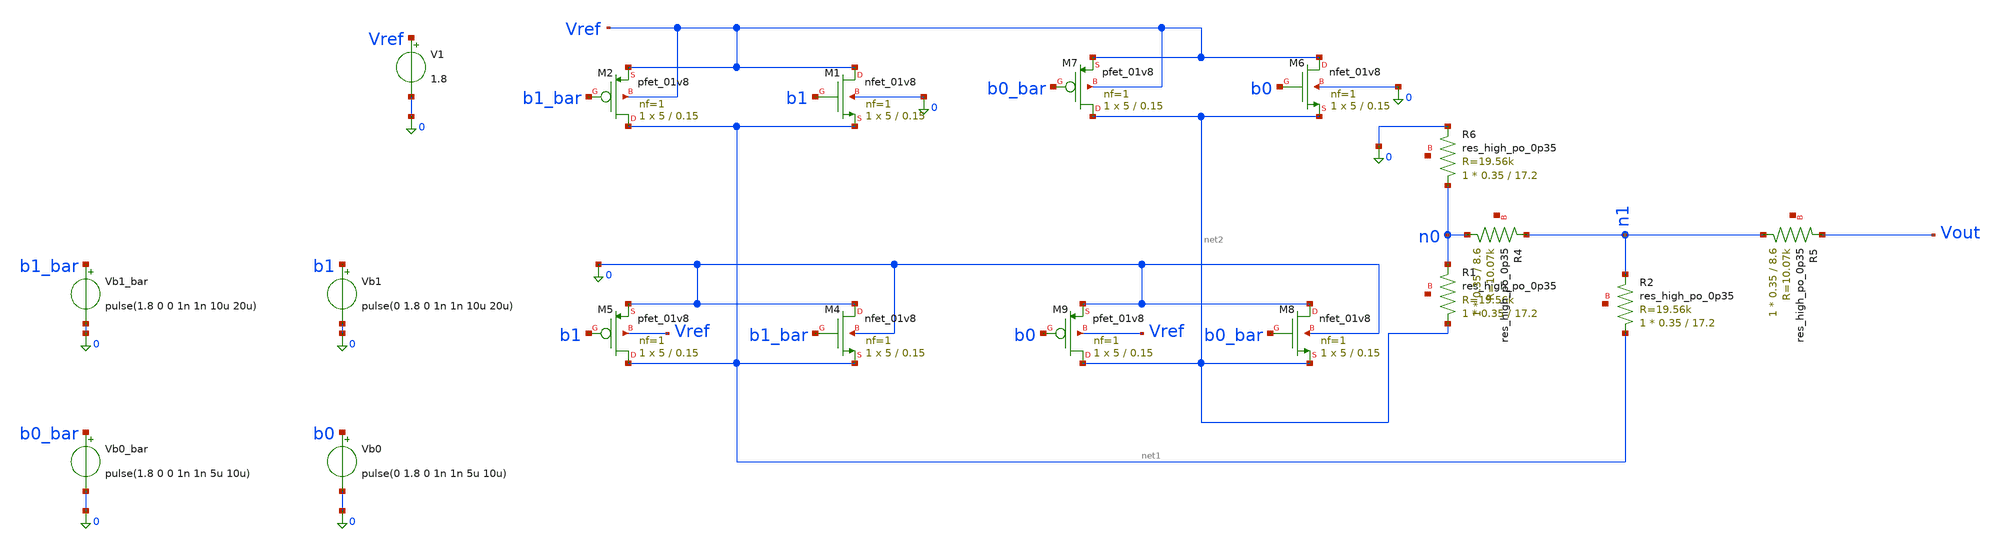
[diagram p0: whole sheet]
** sch_path: sch/dac2bitrapi.sch
**.subckt dac2bitrapi
XM1 Vref b1 net1 0 sky130_fd_pr__nfet_01v8 L=0.15 W=5 nf=1 ad='int((1 + 1)/2) * 5 / 1 * 0.29' as='int((1 + 2)/2) * 5 / 1 * 0.29'
+ pd='2*int((1 + 1)/2) * (5 / 1 + 0.29)' ps='2*int((1 + 2)/2) * (5 / 1 + 0.29)' nrd='0.29 / 5 ' nrs='0.29 / 5 '
+ sa=0 sb=0 sd=0 mult=1 m=1
XM2 net1 b1_bar Vref Vref sky130_fd_pr__pfet_01v8 L=0.15 W=5 nf=1 ad='int((1 + 1)/2) * 5 / 1 * 0.29'
+ as='int((1 + 2)/2) * 5 / 1 * 0.29' pd='2*int((1 + 1)/2) * (5 / 1 + 0.29)' ps='2*int((1 + 2)/2) * (5 / 1 + 0.29)'
+ nrd='0.29 / 5 ' nrs='0.29 / 5 ' sa=0 sb=0 sd=0 mult=1 m=1
XM4 0 b1_bar net1 0 sky130_fd_pr__nfet_01v8 L=0.15 W=5 nf=1 ad='int((1 + 1)/2) * 5 / 1 * 0.29' as='int((1 + 2)/2) * 5 / 1 * 0.29'
+ pd='2*int((1 + 1)/2) * (5 / 1 + 0.29)' ps='2*int((1 + 2)/2) * (5 / 1 + 0.29)' nrd='0.29 / 5 ' nrs='0.29 / 5 '
+ sa=0 sb=0 sd=0 mult=1 m=1
XM5 net1 b1 0 Vref sky130_fd_pr__pfet_01v8 L=0.15 W=5 nf=1 ad='int((1 + 1)/2) * 5 / 1 * 0.29' as='int((1 + 2)/2) * 5 / 1 * 0.29'
+ pd='2*int((1 + 1)/2) * (5 / 1 + 0.29)' ps='2*int((1 + 2)/2) * (5 / 1 + 0.29)' nrd='0.29 / 5 ' nrs='0.29 / 5 '
+ sa=0 sb=0 sd=0 mult=1 m=1
XM6 Vref b0 net2 0 sky130_fd_pr__nfet_01v8 L=0.15 W=5 nf=1 ad='int((1 + 1)/2) * 5 / 1 * 0.29' as='int((1 + 2)/2) * 5 / 1 * 0.29'
+ pd='2*int((1 + 1)/2) * (5 / 1 + 0.29)' ps='2*int((1 + 2)/2) * (5 / 1 + 0.29)' nrd='0.29 / 5 ' nrs='0.29 / 5 '
+ sa=0 sb=0 sd=0 mult=1 m=1
XM7 net2 b0_bar Vref Vref sky130_fd_pr__pfet_01v8 L=0.15 W=5 nf=1 ad='int((1 + 1)/2) * 5 / 1 * 0.29'
+ as='int((1 + 2)/2) * 5 / 1 * 0.29' pd='2*int((1 + 1)/2) * (5 / 1 + 0.29)' ps='2*int((1 + 2)/2) * (5 / 1 + 0.29)'
+ nrd='0.29 / 5 ' nrs='0.29 / 5 ' sa=0 sb=0 sd=0 mult=1 m=1
XM8 0 b0_bar net2 0 sky130_fd_pr__nfet_01v8 L=0.15 W=5 nf=1 ad='int((1 + 1)/2) * 5 / 1 * 0.29' as='int((1 + 2)/2) * 5 / 1 * 0.29'
+ pd='2*int((1 + 1)/2) * (5 / 1 + 0.29)' ps='2*int((1 + 2)/2) * (5 / 1 + 0.29)' nrd='0.29 / 5 ' nrs='0.29 / 5 '
+ sa=0 sb=0 sd=0 mult=1 m=1
XM9 net2 b0 0 Vref sky130_fd_pr__pfet_01v8 L=0.15 W=5 nf=1 ad='int((1 + 1)/2) * 5 / 1 * 0.29' as='int((1 + 2)/2) * 5 / 1 * 0.29'
+ pd='2*int((1 + 1)/2) * (5 / 1 + 0.29)' ps='2*int((1 + 2)/2) * (5 / 1 + 0.29)' nrd='0.29 / 5 ' nrs='0.29 / 5 '
+ sa=0 sb=0 sd=0 mult=1 m=1
XR1 net2 n0 net3 sky130_fd_pr__res_high_po_0p35 L=17.2 mult=1 m=1
XR2 net1 n1 net4 sky130_fd_pr__res_high_po_0p35 L=17.2 mult=1 m=1
V1 Vref 0 1.8
Vb1_bar b1_bar 0 pulse(1.8 0 0 1n 1n 10u 20u)
Vb1 b1 0 pulse(0 1.8 0 1n 1n 10u 20u)
Vb0_bar b0_bar 0 pulse(1.8 0 0 1n 1n 5u 10u)
Vb0 b0 0 pulse(0 1.8 0 1n 1n 5u 10u)
XR4 n0 n1 net5 sky130_fd_pr__res_high_po_0p35 L=8.6 mult=1 m=1
XR5 n1 Vout net6 sky130_fd_pr__res_high_po_0p35 L=8.6 mult=1 m=1
XR6 n0 0 net7 sky130_fd_pr__res_high_po_0p35 L=17.2 mult=1 m=1
**** begin user architecture code


.lib /foss/pdks/ciel/sky130/versions/7b70722e33c03fcb5dabcf4d479fb0822d9251c9/sky130A/libs.tech/ngspice/sky130.lib.spice tt

.options method=gear
.options gmin=1e-12
.options abstol=1e-12 reltol=1e-3

.ic v(net1)=0 v(net2)=0 v(Vout)=0
.tran 0.1u 80u uic

.control
run
let n1_shift = v(n1) + 1
let n0_shift = v(n0) + 2
plot v(Vout) n1_shift n0_shift
.endc


**** end user architecture code
**.ends
.end
